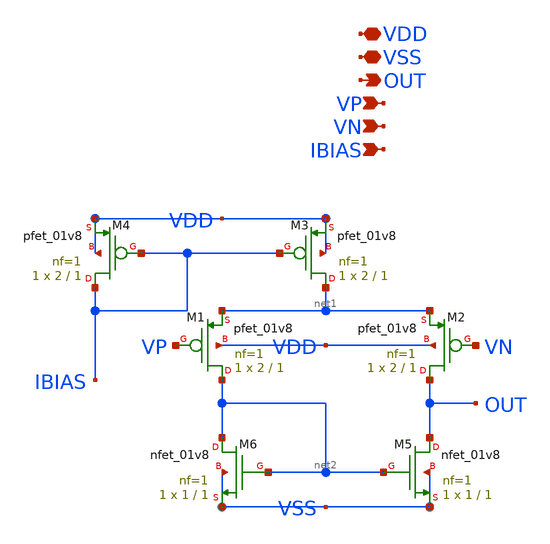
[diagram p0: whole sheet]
** sch_path: designs/libs/core_analog/p-ota/p-ota.sch
**.subckt p-ota VDD VSS VP VN OUT IBIAS
*.iopin VDD
*.iopin VSS
*.ipin VP
*.ipin VN
*.opin OUT
*.ipin IBIAS
XM1 net2 VP net1 VDD sky130_fd_pr__pfet_01v8 L=1 W=2 nf=1 ad='int((nf+1)/2) * W/nf * 0.29' as='int((nf+2)/2) * W/nf * 0.29'
+ pd='2*int((nf+1)/2) * (W/nf + 0.29)' ps='2*int((nf+2)/2) * (W/nf + 0.29)' nrd='0.29 / W' nrs='0.29 / W'
+ sa=0 sb=0 sd=0 mult=1 m=1
XM2 OUT VN net1 VDD sky130_fd_pr__pfet_01v8 L=1 W=2 nf=1 ad='int((nf+1)/2) * W/nf * 0.29' as='int((nf+2)/2) * W/nf * 0.29'
+ pd='2*int((nf+1)/2) * (W/nf + 0.29)' ps='2*int((nf+2)/2) * (W/nf + 0.29)' nrd='0.29 / W' nrs='0.29 / W'
+ sa=0 sb=0 sd=0 mult=1 m=1
XM3 net1 IBIAS VDD VDD sky130_fd_pr__pfet_01v8 L=1 W=2 nf=1 ad='int((nf+1)/2) * W/nf * 0.29' as='int((nf+2)/2) * W/nf * 0.29'
+ pd='2*int((nf+1)/2) * (W/nf + 0.29)' ps='2*int((nf+2)/2) * (W/nf + 0.29)' nrd='0.29 / W' nrs='0.29 / W'
+ sa=0 sb=0 sd=0 mult=1 m=1
XM4 IBIAS IBIAS VDD VDD sky130_fd_pr__pfet_01v8 L=1 W=2 nf=1 ad='int((nf+1)/2) * W/nf * 0.29' as='int((nf+2)/2) * W/nf * 0.29'
+ pd='2*int((nf+1)/2) * (W/nf + 0.29)' ps='2*int((nf+2)/2) * (W/nf + 0.29)' nrd='0.29 / W' nrs='0.29 / W'
+ sa=0 sb=0 sd=0 mult=1 m=1
XM5 OUT net2 VSS VSS sky130_fd_pr__nfet_01v8 L=1 W=1 nf=1 ad='int((nf+1)/2) * W/nf * 0.29' as='int((nf+2)/2) * W/nf * 0.29'
+ pd='2*int((nf+1)/2) * (W/nf + 0.29)' ps='2*int((nf+2)/2) * (W/nf + 0.29)' nrd='0.29 / W' nrs='0.29 / W'
+ sa=0 sb=0 sd=0 mult=1 m=1
XM6 net2 net2 VSS VSS sky130_fd_pr__nfet_01v8 L=1 W=1 nf=1 ad='int((nf+1)/2) * W/nf * 0.29' as='int((nf+2)/2) * W/nf * 0.29'
+ pd='2*int((nf+1)/2) * (W/nf + 0.29)' ps='2*int((nf+2)/2) * (W/nf + 0.29)' nrd='0.29 / W' nrs='0.29 / W'
+ sa=0 sb=0 sd=0 mult=1 m=1
**.ends
.end
